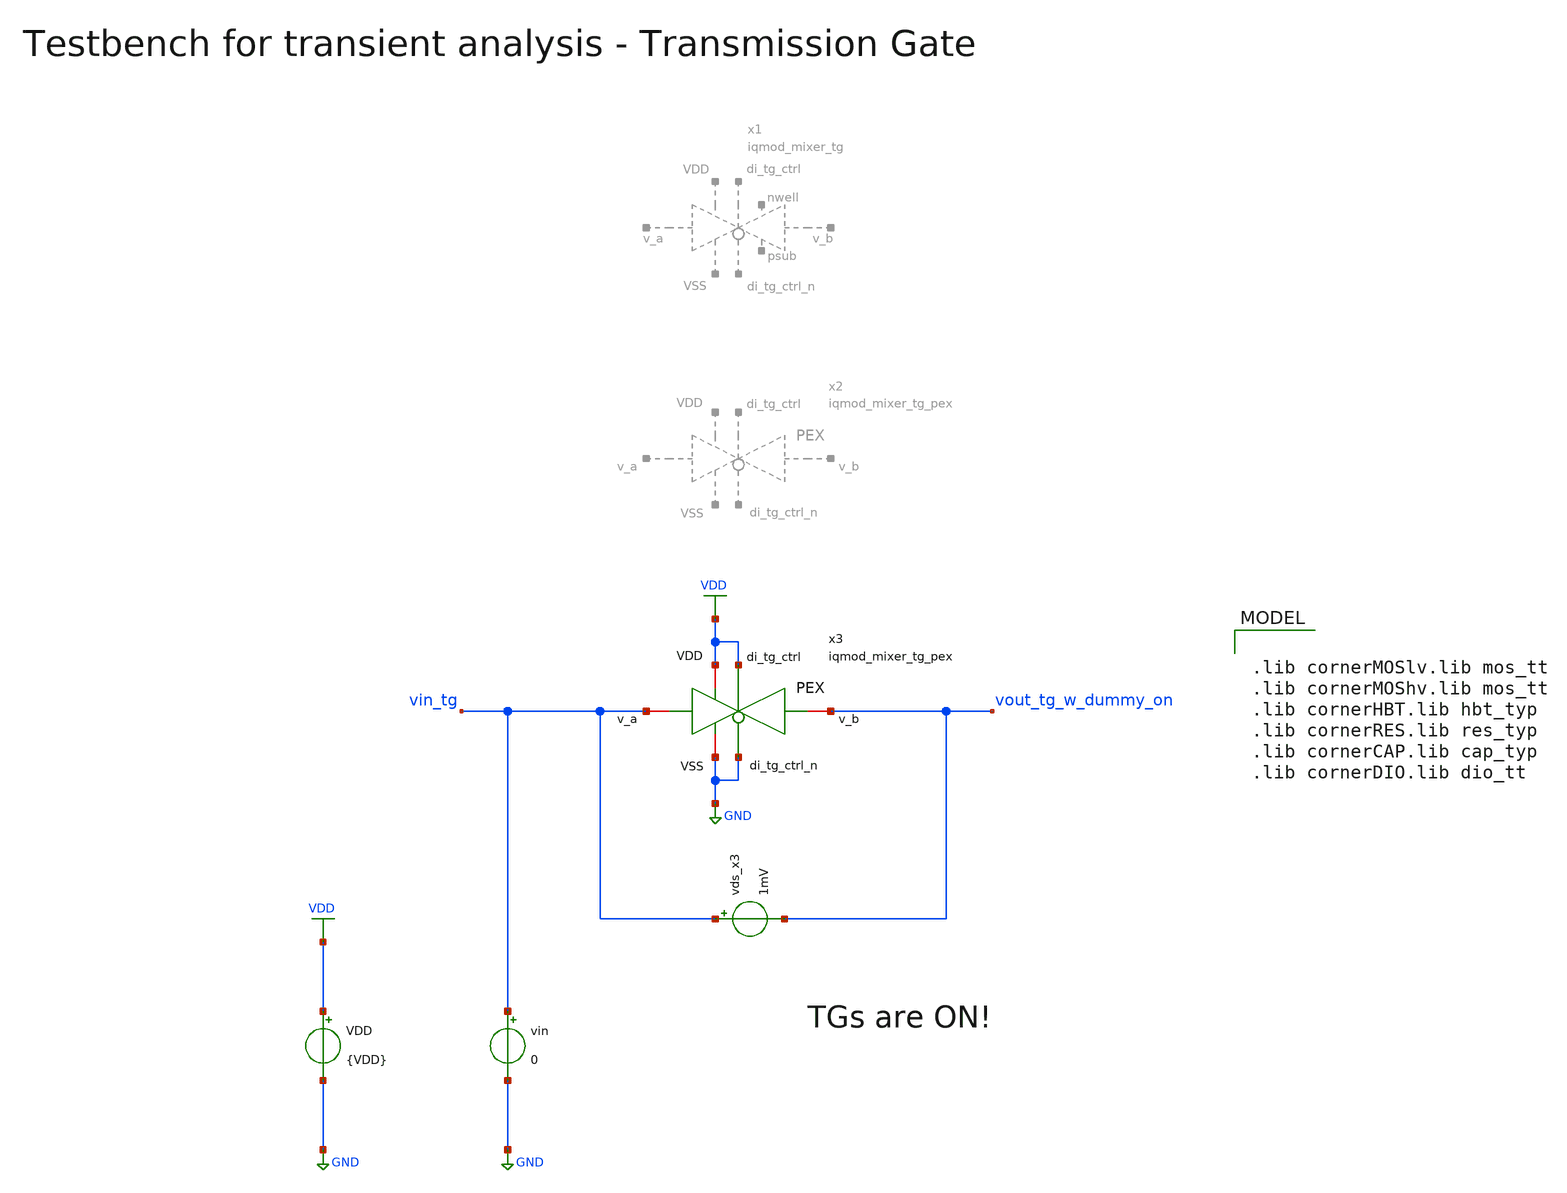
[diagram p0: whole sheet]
** sch_path: ihp130/macros/iqmod/xschem/testbenches/iqmod_mixer_tg_tb_dc_Ron.sch
**.subckt iqmod_mixer_tg_tb_dc_Ron
VDD VDD GND {VDD}
vin vin_tg GND 0
vds_x3 vin_tg vout_tg_w_dummy_on 1mV
x3 VDD GND GND VDD vin_tg vout_tg_w_dummy_on iqmod_mixer_tg_pex
**** begin user architecture code


.include ../../verification/pex/iqmod_mixer_tg_pex.spice
.param VDD=1.5
.csparam VDD=VDD
.param Vcm=VDD/2
.param temp=27
.param Cload=10p
.options savecurrents method=gear reltol=1e-3 abstol=1e-15 gmin=1e-15
.control

save all

* Operating Point Analysis
op
remzerovec
write iqmod_mixer_tg_tb_dc_Ron.raw
set appendwrite

* DC Sweep Analysis
dc vin 0 $&VDD 0.01
write iqmod_mixer_tg_tb_dc_Ron.raw

* On-Resistance
* LV with Dummy
let r_w_dummy_on = (v(vout_tg_w_dummy_on)-v(vin_tg))/I(vds_x3)
plot r_w_dummy_on xlabel 'Vin in V' ylabel 'Ron with Dummy in Ohm'

* Writing Data
unset appendwrite
set wr_singlescale
set wr_vecnames
wrdata $PROJECT_PATH/python/plot_simulations/data/iqmod_mixer_tg_tb_dc_Ron.txt v(r_w_dummy_on)

*quit
.endc


.lib cornerMOSlv.lib mos_tt
.lib cornerMOShv.lib mos_tt
.lib cornerHBT.lib hbt_typ
.lib cornerRES.lib res_typ
.lib cornerCAP.lib cap_typ
.lib cornerDIO.lib dio_tt

**** end user architecture code
**.ends

* expanding   symbol:  iqmod_mixer_tg.sym # of pins=8
** sym_path: ihp130/macros/iqmod/xschem/iqmod_mixer_tg.sym
** sch_path: ihp130/macros/iqmod/xschem/iqmod_mixer_tg.sch
.subckt iqmod_mixer_tg nwell psub VDD di_tg_ctrl VSS v_b v_a di_tg_ctrl_n
*.iopin v_a
*.iopin v_b
*.ipin di_tg_ctrl
*.ipin di_tg_ctrl_n
*.iopin VDD
*.iopin VSS
*.iopin nwell
*.iopin psub
XM1 v_a di_tg_ctrl v_b psub sg13_lv_nmos w=108.0u l=0.13u ng=36 m=1 mm_ok=1
XM2 v_a di_tg_ctrl_n v_b nwell sg13_lv_pmos w=324.0u l=0.13u ng=36 m=1 mm_ok=1
XMdummy2 v_b di_tg_ctrl v_b nwell sg13_lv_pmos w=162.0u l=0.13u ng=18 m=1 mm_ok=1
XMdummy1 v_b di_tg_ctrl_n v_b psub sg13_lv_nmos w=54.0u l=0.13u ng=18 m=1 mm_ok=1
XR1 VDD nwell ntap1 R=2.829 w=29.86e-6 l=11.02e-6 rw=0.3e-6
XR2 VSS psub ptap1 R=3.29 w=29.86e-6 l=5.38e-6 rw=0.3e-6
.ends

.GLOBAL GND
.GLOBAL VDD
.end
